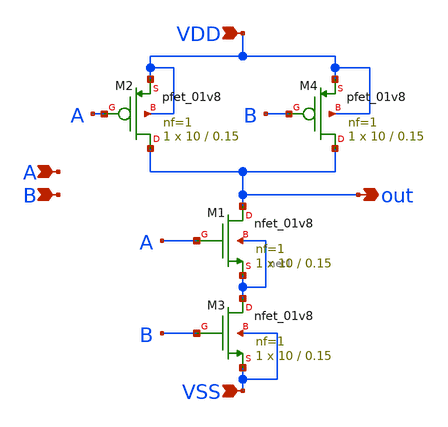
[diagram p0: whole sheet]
** sch_path: nand/nand2.sch
**.subckt nand2 VDD A B VSS out
*.ipin VDD
*.ipin A
*.ipin B
*.ipin VSS
*.opin out
XM1 out A net1 net1 sky130_fd_pr__nfet_01v8 L=0.15 W=10 nf=1 ad='int((nf+1)/2) * W/nf * 0.29' as='int((nf+2)/2) * W/nf * 0.29'
+ pd='2*int((nf+1)/2) * (W/nf + 0.29)' ps='2*int((nf+2)/2) * (W/nf + 0.29)' nrd='0.29 / W' nrs='0.29 / W'
+ sa=0 sb=0 sd=0 mult=1 m=1
XM2 out A VDD VDD sky130_fd_pr__pfet_01v8 L=0.15 W=10 nf=1 ad='int((nf+1)/2) * W/nf * 0.29' as='int((nf+2)/2) * W/nf * 0.29'
+ pd='2*int((nf+1)/2) * (W/nf + 0.29)' ps='2*int((nf+2)/2) * (W/nf + 0.29)' nrd='0.29 / W' nrs='0.29 / W'
+ sa=0 sb=0 sd=0 mult=1 m=1
XM3 net1 B VSS VSS sky130_fd_pr__nfet_01v8 L=0.15 W=10 nf=1 ad='int((nf+1)/2) * W/nf * 0.29' as='int((nf+2)/2) * W/nf * 0.29'
+ pd='2*int((nf+1)/2) * (W/nf + 0.29)' ps='2*int((nf+2)/2) * (W/nf + 0.29)' nrd='0.29 / W' nrs='0.29 / W'
+ sa=0 sb=0 sd=0 mult=1 m=1
XM4 out B VDD VDD sky130_fd_pr__pfet_01v8 L=0.15 W=10 nf=1 ad='int((nf+1)/2) * W/nf * 0.29' as='int((nf+2)/2) * W/nf * 0.29'
+ pd='2*int((nf+1)/2) * (W/nf + 0.29)' ps='2*int((nf+2)/2) * (W/nf + 0.29)' nrd='0.29 / W' nrs='0.29 / W'
+ sa=0 sb=0 sd=0 mult=1 m=1
**.ends
.end
